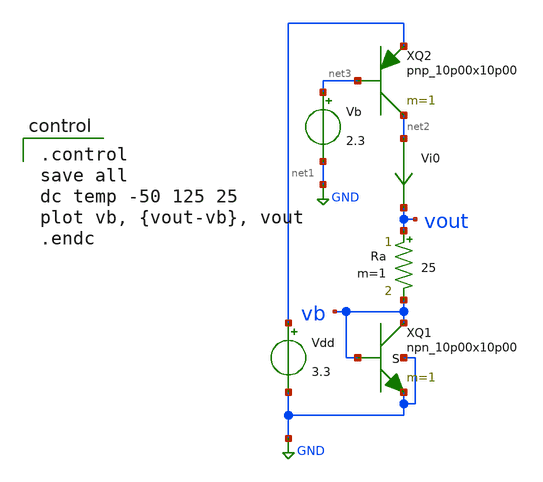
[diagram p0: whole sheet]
** sch_path: bgr/npn-diode-tcomp.sch
**.subckt npn-diode-tcomp
XQ1 vb vb GND GND npn_10p00x10p00 m=1
Vdd net1 GND 3.3
Ra vout vb 25 m=1
Vi0 net2 vout 0
.save i(vi0)
XQ2 net2 net3 net1 pnp_10p00x10p00 m=1
Vb net3 GND 2.3
**** begin user architecture code

.include $::180MCU_MODELS/design.ngspice
.lib $::180MCU_MODELS/sm141064.ngspice typical
.lib $::180MCU_MODELS/sm141064.ngspice res_typical
.lib $::180MCU_MODELS/sm141064.ngspice moscap_typical
.lib $::180MCU_MODELS/sm141064.ngspice bjt_typical
* .lib $::180MCU_MODELS/sm141064.ngspice res_statistical


.control
save all
dc temp -50 125 25
plot vb, {vout-vb}, vout
.endc

**** end user architecture code
**.ends
.GLOBAL GND
.end
